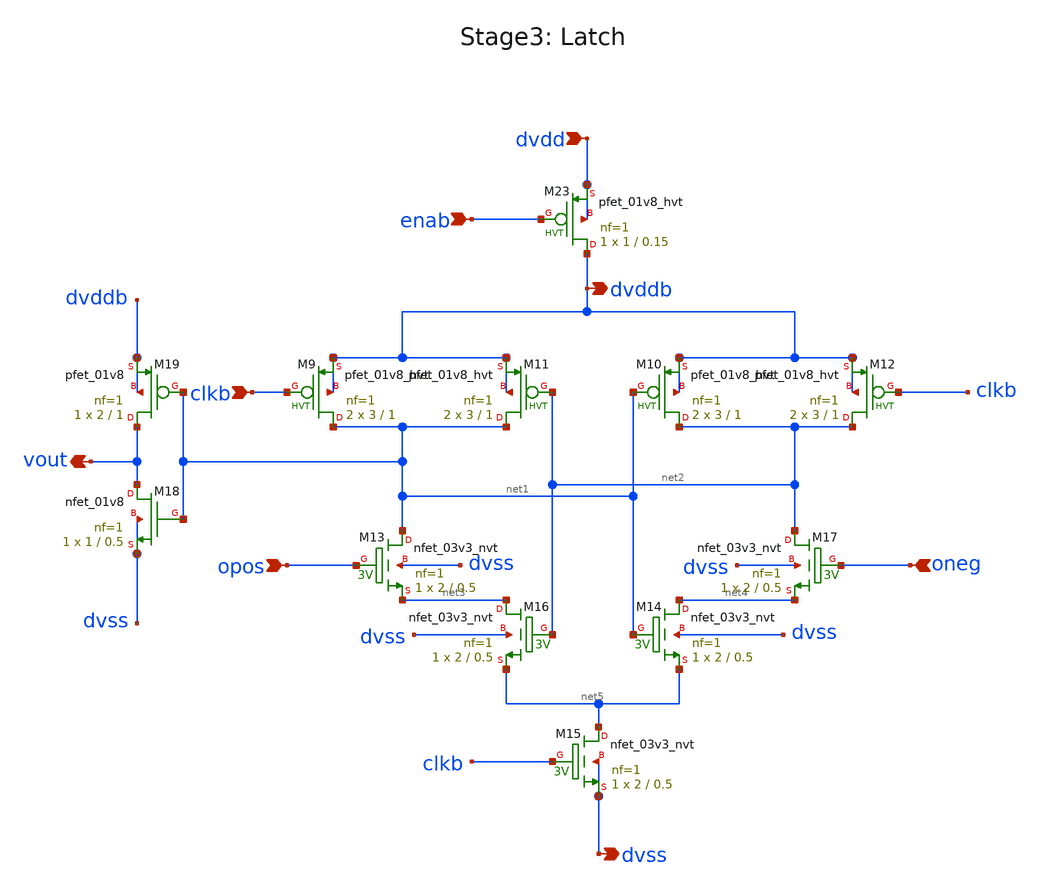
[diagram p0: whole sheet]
** sch_path: xschem/Stage2_latch.sch
**.subckt Stage2_latch clkb vout dvss dvdd opos oneg enab dvddb
*.ipin clkb
*.opin vout
*.opin dvss
*.ipin dvdd
*.ipin opos
*.ipin oneg
*.ipin enab
*.opin dvddb
XM18 vout net1 dvss dvss sky130_fd_pr__nfet_01v8 L=0.5 W=1 nf=1 ad='int((nf+1)/2) * W/nf * 0.29' as='int((nf+2)/2) * W/nf * 0.29'
+ pd='2*int((nf+1)/2) * (W/nf + 0.29)' ps='2*int((nf+2)/2) * (W/nf + 0.29)' nrd='0.29 / W' nrs='0.29 / W'
+ sa=0 sb=0 sd=0 mult=1 m=1
XM19 vout net1 dvddb dvddb sky130_fd_pr__pfet_01v8 L=1 W=2 nf=1 ad='int((nf+1)/2) * W/nf * 0.29' as='int((nf+2)/2) * W/nf * 0.29'
+ pd='2*int((nf+1)/2) * (W/nf + 0.29)' ps='2*int((nf+2)/2) * (W/nf + 0.29)' nrd='0.29 / W' nrs='0.29 / W'
+ sa=0 sb=0 sd=0 mult=1 m=1
XM13 net1 opos net3 dvss sky130_fd_pr__nfet_03v3_nvt L=0.5 W=2 nf=1 ad='int((nf+1)/2) * W/nf * 0.29'
+ as='int((nf+2)/2) * W/nf * 0.29' pd='2*int((nf+1)/2) * (W/nf + 0.29)' ps='2*int((nf+2)/2) * (W/nf + 0.29)'
+ nrd='0.29 / W' nrs='0.29 / W' sa=0 sb=0 sd=0 mult=1 m=1
XM14 net4 net1 net5 dvss sky130_fd_pr__nfet_03v3_nvt L=0.5 W=2 nf=1 ad='int((nf+1)/2) * W/nf * 0.29'
+ as='int((nf+2)/2) * W/nf * 0.29' pd='2*int((nf+1)/2) * (W/nf + 0.29)' ps='2*int((nf+2)/2) * (W/nf + 0.29)'
+ nrd='0.29 / W' nrs='0.29 / W' sa=0 sb=0 sd=0 mult=1 m=1
XM15 net5 clkb dvss dvss sky130_fd_pr__nfet_03v3_nvt L=0.5 W=2 nf=1 ad='int((nf+1)/2) * W/nf * 0.29'
+ as='int((nf+2)/2) * W/nf * 0.29' pd='2*int((nf+1)/2) * (W/nf + 0.29)' ps='2*int((nf+2)/2) * (W/nf + 0.29)'
+ nrd='0.29 / W' nrs='0.29 / W' sa=0 sb=0 sd=0 mult=1 m=1
XM16 net3 net2 net5 dvss sky130_fd_pr__nfet_03v3_nvt L=0.5 W=2 nf=1 ad='int((nf+1)/2) * W/nf * 0.29'
+ as='int((nf+2)/2) * W/nf * 0.29' pd='2*int((nf+1)/2) * (W/nf + 0.29)' ps='2*int((nf+2)/2) * (W/nf + 0.29)'
+ nrd='0.29 / W' nrs='0.29 / W' sa=0 sb=0 sd=0 mult=1 m=1
XM17 net2 oneg net4 dvss sky130_fd_pr__nfet_03v3_nvt L=0.5 W=2 nf=1 ad='int((nf+1)/2) * W/nf * 0.29'
+ as='int((nf+2)/2) * W/nf * 0.29' pd='2*int((nf+1)/2) * (W/nf + 0.29)' ps='2*int((nf+2)/2) * (W/nf + 0.29)'
+ nrd='0.29 / W' nrs='0.29 / W' sa=0 sb=0 sd=0 mult=1 m=1
XM23 dvddb enab dvdd dvdd sky130_fd_pr__pfet_01v8_hvt L=0.15 W=1 nf=1 ad='int((nf+1)/2) * W/nf * 0.29'
+ as='int((nf+2)/2) * W/nf * 0.29' pd='2*int((nf+1)/2) * (W/nf + 0.29)' ps='2*int((nf+2)/2) * (W/nf + 0.29)'
+ nrd='0.29 / W' nrs='0.29 / W' sa=0 sb=0 sd=0 mult=1 m=1
XM9 net1 clkb dvddb dvddb sky130_fd_pr__pfet_01v8_hvt L=1 W=3 nf=1 ad='int((nf+1)/2) * W/nf * 0.29' as='int((nf+2)/2) * W/nf * 0.29'
+ pd='2*int((nf+1)/2) * (W/nf + 0.29)' ps='2*int((nf+2)/2) * (W/nf + 0.29)' nrd='0.29 / W' nrs='0.29 / W'
+ sa=0 sb=0 sd=0 mult=2 m=2
XM10 net2 net1 dvddb dvddb sky130_fd_pr__pfet_01v8_hvt L=1 W=3 nf=1 ad='int((nf+1)/2) * W/nf * 0.29'
+ as='int((nf+2)/2) * W/nf * 0.29' pd='2*int((nf+1)/2) * (W/nf + 0.29)' ps='2*int((nf+2)/2) * (W/nf + 0.29)'
+ nrd='0.29 / W' nrs='0.29 / W' sa=0 sb=0 sd=0 mult=2 m=2
XM11 net1 net2 dvddb dvddb sky130_fd_pr__pfet_01v8_hvt L=1 W=3 nf=1 ad='int((nf+1)/2) * W/nf * 0.29'
+ as='int((nf+2)/2) * W/nf * 0.29' pd='2*int((nf+1)/2) * (W/nf + 0.29)' ps='2*int((nf+2)/2) * (W/nf + 0.29)'
+ nrd='0.29 / W' nrs='0.29 / W' sa=0 sb=0 sd=0 mult=2 m=2
XM12 net2 clkb dvddb dvddb sky130_fd_pr__pfet_01v8_hvt L=1 W=3 nf=1 ad='int((nf+1)/2) * W/nf * 0.29'
+ as='int((nf+2)/2) * W/nf * 0.29' pd='2*int((nf+1)/2) * (W/nf + 0.29)' ps='2*int((nf+2)/2) * (W/nf + 0.29)'
+ nrd='0.29 / W' nrs='0.29 / W' sa=0 sb=0 sd=0 mult=2 m=2
**.ends
.end
